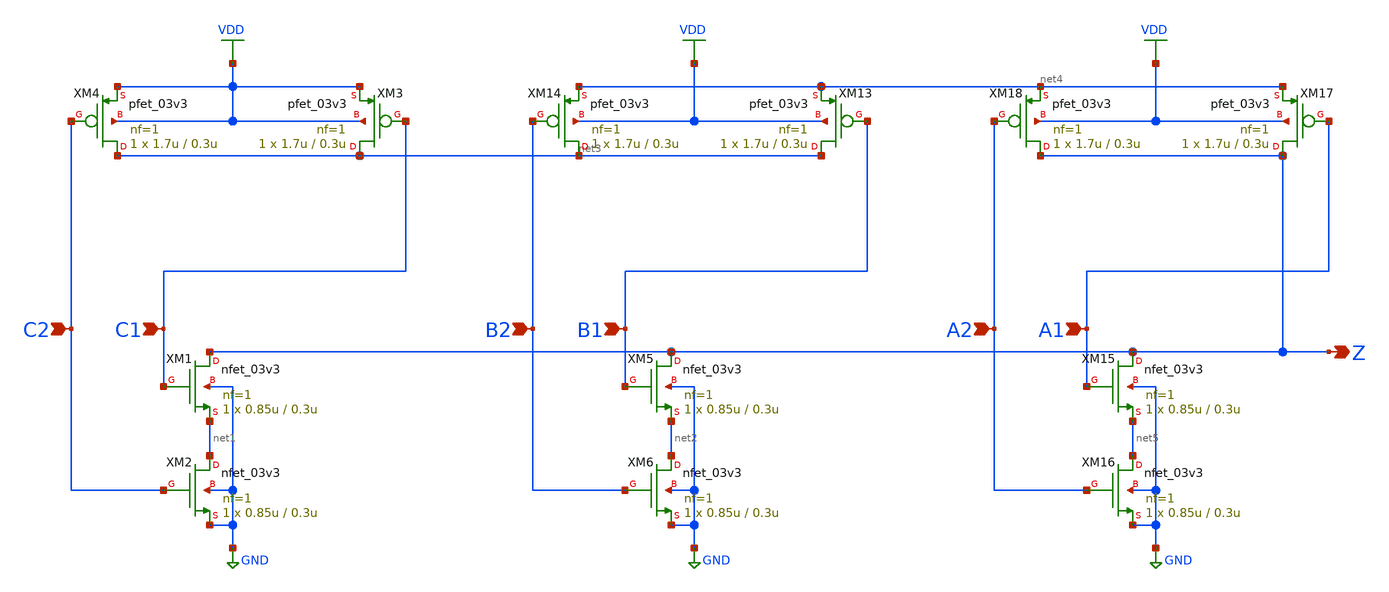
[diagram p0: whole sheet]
** sch_path: globalfoundries-pdk-libs-gf180mcu_sah_sc/cells/aoi222/gf180mcu_sah_sc_aoi222_1.sch
**.subckt gf180mcu_sah_sc_aoi222_1 C1 C2 B1 B2 Z A1 A2
*.ipin C1
*.ipin C2
*.ipin B1
*.ipin B2
*.opin Z
*.ipin A1
*.ipin A2
XM1 Z C1 net1 GND nfet_03v3 L=0.3u W=0.85u nf=1 ad='int((nf+1)/2) * W/nf * 0.18u' as='int((nf+2)/2) * W/nf * 0.18u'
+ pd='2*int((nf+1)/2) * (W/nf + 0.18u)' ps='2*int((nf+2)/2) * (W/nf + 0.18u)' nrd='0.18u / W' nrs='0.18u / W'
+ sa=0 sb=0 sd=0 m=1
XM2 net1 C2 GND GND nfet_03v3 L=0.3u W=0.85u nf=1 ad='int((nf+1)/2) * W/nf * 0.18u' as='int((nf+2)/2) * W/nf * 0.18u'
+ pd='2*int((nf+1)/2) * (W/nf + 0.18u)' ps='2*int((nf+2)/2) * (W/nf + 0.18u)' nrd='0.18u / W' nrs='0.18u / W'
+ sa=0 sb=0 sd=0 m=1
XM3 net3 C1 VDD VDD pfet_03v3 L=0.3u W=1.7u nf=1 ad='int((nf+1)/2) * W/nf * 0.18u' as='int((nf+2)/2) * W/nf * 0.18u'
+ pd='2*int((nf+1)/2) * (W/nf + 0.18u)' ps='2*int((nf+2)/2) * (W/nf + 0.18u)' nrd='0.18u / W' nrs='0.18u / W'
+ sa=0 sb=0 sd=0 m=1
XM4 net3 C2 VDD VDD pfet_03v3 L=0.3u W=1.7u nf=1 ad='int((nf+1)/2) * W/nf * 0.18u' as='int((nf+2)/2) * W/nf * 0.18u'
+ pd='2*int((nf+1)/2) * (W/nf + 0.18u)' ps='2*int((nf+2)/2) * (W/nf + 0.18u)' nrd='0.18u / W' nrs='0.18u / W'
+ sa=0 sb=0 sd=0 m=1
XM5 Z B1 net2 GND nfet_03v3 L=0.3u W=0.85u nf=1 ad='int((nf+1)/2) * W/nf * 0.18u' as='int((nf+2)/2) * W/nf * 0.18u'
+ pd='2*int((nf+1)/2) * (W/nf + 0.18u)' ps='2*int((nf+2)/2) * (W/nf + 0.18u)' nrd='0.18u / W' nrs='0.18u / W'
+ sa=0 sb=0 sd=0 m=1
XM6 net2 B2 GND GND nfet_03v3 L=0.3u W=0.85u nf=1 ad='int((nf+1)/2) * W/nf * 0.18u' as='int((nf+2)/2) * W/nf * 0.18u'
+ pd='2*int((nf+1)/2) * (W/nf + 0.18u)' ps='2*int((nf+2)/2) * (W/nf + 0.18u)' nrd='0.18u / W' nrs='0.18u / W'
+ sa=0 sb=0 sd=0 m=1
XM13 net3 B1 net4 VDD pfet_03v3 L=0.3u W=1.7u nf=1 ad='int((nf+1)/2) * W/nf * 0.18u' as='int((nf+2)/2) * W/nf * 0.18u'
+ pd='2*int((nf+1)/2) * (W/nf + 0.18u)' ps='2*int((nf+2)/2) * (W/nf + 0.18u)' nrd='0.18u / W' nrs='0.18u / W'
+ sa=0 sb=0 sd=0 m=1
XM14 net3 B2 net4 VDD pfet_03v3 L=0.3u W=1.7u nf=1 ad='int((nf+1)/2) * W/nf * 0.18u' as='int((nf+2)/2) * W/nf * 0.18u'
+ pd='2*int((nf+1)/2) * (W/nf + 0.18u)' ps='2*int((nf+2)/2) * (W/nf + 0.18u)' nrd='0.18u / W' nrs='0.18u / W'
+ sa=0 sb=0 sd=0 m=1
XM15 Z A1 net5 GND nfet_03v3 L=0.3u W=0.85u nf=1 ad='int((nf+1)/2) * W/nf * 0.18u' as='int((nf+2)/2) * W/nf * 0.18u'
+ pd='2*int((nf+1)/2) * (W/nf + 0.18u)' ps='2*int((nf+2)/2) * (W/nf + 0.18u)' nrd='0.18u / W' nrs='0.18u / W'
+ sa=0 sb=0 sd=0 m=1
XM16 net5 A2 GND GND nfet_03v3 L=0.3u W=0.85u nf=1 ad='int((nf+1)/2) * W/nf * 0.18u' as='int((nf+2)/2) * W/nf * 0.18u'
+ pd='2*int((nf+1)/2) * (W/nf + 0.18u)' ps='2*int((nf+2)/2) * (W/nf + 0.18u)' nrd='0.18u / W' nrs='0.18u / W'
+ sa=0 sb=0 sd=0 m=1
XM17 Z A1 net4 VDD pfet_03v3 L=0.3u W=1.7u nf=1 ad='int((nf+1)/2) * W/nf * 0.18u' as='int((nf+2)/2) * W/nf * 0.18u'
+ pd='2*int((nf+1)/2) * (W/nf + 0.18u)' ps='2*int((nf+2)/2) * (W/nf + 0.18u)' nrd='0.18u / W' nrs='0.18u / W'
+ sa=0 sb=0 sd=0 m=1
XM18 Z A2 net4 VDD pfet_03v3 L=0.3u W=1.7u nf=1 ad='int((nf+1)/2) * W/nf * 0.18u' as='int((nf+2)/2) * W/nf * 0.18u'
+ pd='2*int((nf+1)/2) * (W/nf + 0.18u)' ps='2*int((nf+2)/2) * (W/nf + 0.18u)' nrd='0.18u / W' nrs='0.18u / W'
+ sa=0 sb=0 sd=0 m=1
**.ends
.GLOBAL GND
.GLOBAL VDD
.end
